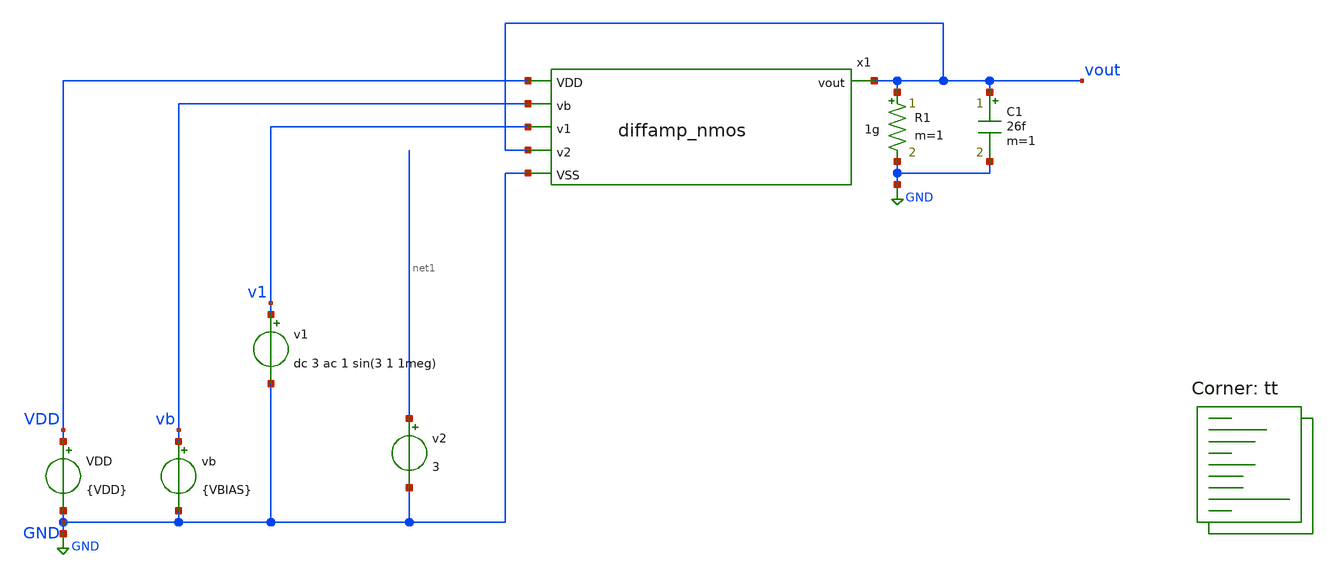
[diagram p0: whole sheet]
** sch_path: xschem/tb_diffamp_nmos_ac.sch
**.subckt tb_diffamp_nmos_ac
x1 v1 vout GND VDD vb vout diffamp_nmos
VDD VDD GND {VDD}
vb vb GND {VBIAS}
v1 v1 GND dc 3 ac 1 sin(3 1 1meg)
R1 vout GND 1g m=1
v2 net1 GND 3
C1 vout GND 26f m=1
**** begin user architecture code
.lib $::SKYWATER_MODELS/sky130.lib.spice tt



.options reltol=0.0001 abstol=10e-15
*.include diffamp_nmos.spice
.param VDD=6
.param VSS=0
.param VBIAS=1
.options savecurrents
* .options reltol=0.01 abstol=10e-12
.control
  save all
  op
  remzerovec
  write tb_diffamp_nmos_ac.raw
  set appendwrite
  * ac sweep
  ac dec 20 1 1gig
  remzerovec
  write tb_diffamp_nmos_ac.raw
  * tran
  tran 1n 5u
  remzerovec
  write tb_diffamp_nmos_ac.raw
.endc



**** end user architecture code
**.ends

* expanding   symbol:  diffamp_nmos.sym # of pins=6
** sym_path: xschem/diffamp_nmos.sym
** sch_path: xschem/diffamp_nmos.sch
.subckt diffamp_nmos v1 v2 VSS VDD vb vout
*.ipin v1
*.ipin v2
*.ipin vb
*.opin vout
*.ipin VDD
*.ipin VSS
XM7 int2 int3 VDD VDD sky130_fd_pr__pfet_g5v0d10v5 L=1 W=1.5 nf=1 ad='int((nf+1)/2) * W/nf * 0.29' as='int((nf+2)/2) * W/nf * 0.29'
+ pd='2*int((nf+1)/2) * (W/nf + 0.29)' ps='2*int((nf+2)/2) * (W/nf + 0.29)' nrd='0.29 / W' nrs='0.29 / W'
+ sa=0 sb=0 sd=0 mult=1 m=1
XM8 int2 int2 VSS VSS sky130_fd_pr__nfet_g5v0d10v5 L=1 W=1.5 nf=1 ad='int((nf+1)/2) * W/nf * 0.29' as='int((nf+2)/2) * W/nf * 0.29'
+ pd='2*int((nf+1)/2) * (W/nf + 0.29)' ps='2*int((nf+2)/2) * (W/nf + 0.29)' nrd='0.29 / W' nrs='0.29 / W'
+ sa=0 sb=0 sd=0 mult=1 m=1
XM9 vout int2 VSS VSS sky130_fd_pr__nfet_g5v0d10v5 L=1 W=1.5 nf=1 ad='int((nf+1)/2) * W/nf * 0.29' as='int((nf+2)/2) * W/nf * 0.29'
+ pd='2*int((nf+1)/2) * (W/nf + 0.29)' ps='2*int((nf+2)/2) * (W/nf + 0.29)' nrd='0.29 / W' nrs='0.29 / W'
+ sa=0 sb=0 sd=0 mult=1 m=1
XM1 int4 v1 int1 VSS sky130_fd_pr__nfet_g5v0d10v5 L=1 W=1.5 nf=1 ad='int((nf+1)/2) * W/nf * 0.29' as='int((nf+2)/2) * W/nf * 0.29'
+ pd='2*int((nf+1)/2) * (W/nf + 0.29)' ps='2*int((nf+2)/2) * (W/nf + 0.29)' nrd='0.29 / W' nrs='0.29 / W'
+ sa=0 sb=0 sd=0 mult=1 m=1
XM2 int3 v2 int1 VSS sky130_fd_pr__nfet_g5v0d10v5 L=1 W=1.5 nf=1 ad='int((nf+1)/2) * W/nf * 0.29' as='int((nf+2)/2) * W/nf * 0.29'
+ pd='2*int((nf+1)/2) * (W/nf + 0.29)' ps='2*int((nf+2)/2) * (W/nf + 0.29)' nrd='0.29 / W' nrs='0.29 / W'
+ sa=0 sb=0 sd=0 mult=1 m=1
XM6 int3 int3 VDD VDD sky130_fd_pr__pfet_g5v0d10v5 L=1 W=1.5 nf=1 ad='int((nf+1)/2) * W/nf * 0.29' as='int((nf+2)/2) * W/nf * 0.29'
+ pd='2*int((nf+1)/2) * (W/nf + 0.29)' ps='2*int((nf+2)/2) * (W/nf + 0.29)' nrd='0.29 / W' nrs='0.29 / W'
+ sa=0 sb=0 sd=0 mult=1 m=1
XM5 vout int4 VDD VDD sky130_fd_pr__pfet_g5v0d10v5 L=1 W=1.5 nf=1 ad='int((nf+1)/2) * W/nf * 0.29' as='int((nf+2)/2) * W/nf * 0.29'
+ pd='2*int((nf+1)/2) * (W/nf + 0.29)' ps='2*int((nf+2)/2) * (W/nf + 0.29)' nrd='0.29 / W' nrs='0.29 / W'
+ sa=0 sb=0 sd=0 mult=1 m=1
XM3a int1 vb int5 VSS sky130_fd_pr__nfet_g5v0d10v5 L=1 W=1.5 nf=1 ad='int((nf+1)/2) * W/nf * 0.29' as='int((nf+2)/2) * W/nf * 0.29'
+ pd='2*int((nf+1)/2) * (W/nf + 0.29)' ps='2*int((nf+2)/2) * (W/nf + 0.29)' nrd='0.29 / W' nrs='0.29 / W'
+ sa=0 sb=0 sd=0 mult=1 m=1
XM3b int5 vb VSS VSS sky130_fd_pr__nfet_g5v0d10v5 L=1 W=1.5 nf=1 ad='int((nf+1)/2) * W/nf * 0.29' as='int((nf+2)/2) * W/nf * 0.29'
+ pd='2*int((nf+1)/2) * (W/nf + 0.29)' ps='2*int((nf+2)/2) * (W/nf + 0.29)' nrd='0.29 / W' nrs='0.29 / W'
+ sa=0 sb=0 sd=0 mult=1 m=1
XM4 int4 int4 VDD VDD sky130_fd_pr__pfet_g5v0d10v5 L=1 W=1.5 nf=1 ad='int((nf+1)/2) * W/nf * 0.29' as='int((nf+2)/2) * W/nf * 0.29'
+ pd='2*int((nf+1)/2) * (W/nf + 0.29)' ps='2*int((nf+2)/2) * (W/nf + 0.29)' nrd='0.29 / W' nrs='0.29 / W'
+ sa=0 sb=0 sd=0 mult=1 m=1
.ends

.GLOBAL GND
.end
